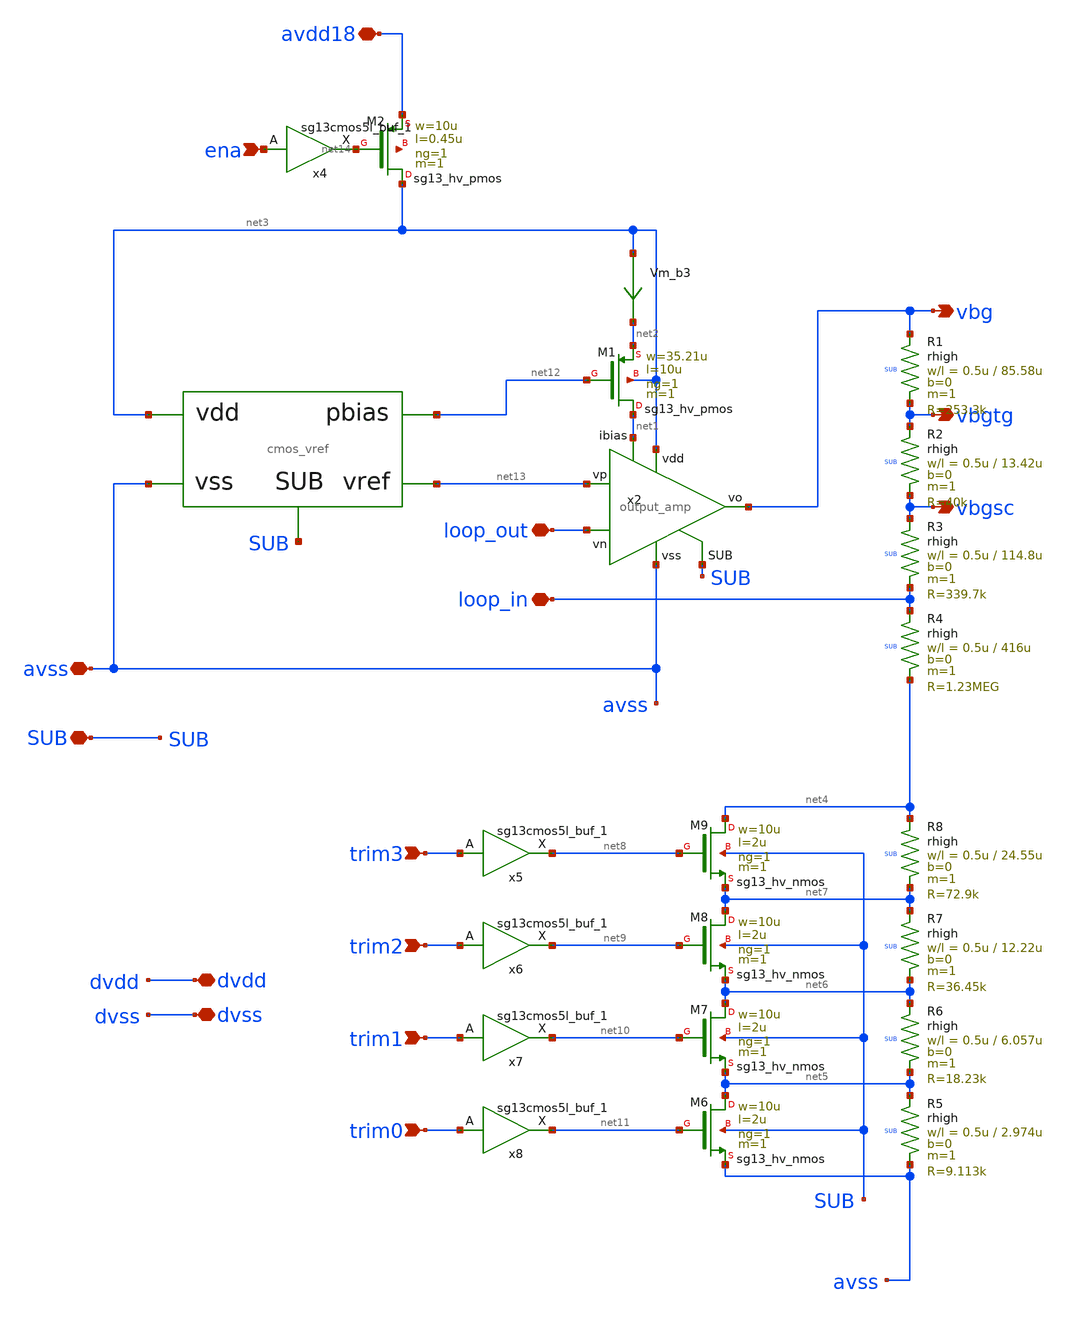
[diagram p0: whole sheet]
** sch_path: release/xschem/sch/top.sch
**.subckt top vbg avss SUB loop_in loop_out dvdd dvss vbgsc vbgtg trim3 trim2 trim1 trim0 avdd18 ena
*.opin vbg
*.iopin avss
*.iopin SUB
*.iopin loop_in
*.iopin loop_out
*.iopin dvdd
*.iopin dvss
*.opin vbgsc
*.opin vbgtg
*.ipin trim3
*.ipin trim2
*.ipin trim1
*.ipin trim0
*.iopin avdd18
*.ipin ena
x2 net3 vbg net13 loop_out net1 avss SUB output_amp
Vm_b3 net3 net2 0
.save i(vm_b3)
XM1 net1 net12 net2 net3 sg13_hv_pmos w=35.21u l=10u ng=1 m=1 mm_ok=1
x5 net8 trim3 dvdd dvss sg13cmos5l_buf_1
x6 net9 trim2 dvdd dvss sg13cmos5l_buf_1
x7 net10 trim1 dvdd dvss sg13cmos5l_buf_1
x8 net11 trim0 dvdd dvss sg13cmos5l_buf_1
XR1 vbg vbgtg SUB rhigh w=0.5u l=85.58u m=1 b=0 mm_ok=1
XR2 vbgtg vbgsc SUB rhigh w=0.5u l=13.42u m=1 b=0 mm_ok=1
XR3 vbgsc loop_in SUB rhigh w=0.5u l=114.8u m=1 b=0 mm_ok=1
XR4 loop_in net4 SUB rhigh w=0.5u l=416u m=1 b=0 mm_ok=1
XM6 net5 net11 avss SUB sg13_hv_nmos w=10u l=2u ng=1 m=1 mm_ok=1
XM7 net6 net10 net5 SUB sg13_hv_nmos w=10u l=2u ng=1 m=1 mm_ok=1
XM8 net7 net9 net6 SUB sg13_hv_nmos w=10u l=2u ng=1 m=1 mm_ok=1
XM9 net4 net8 net7 SUB sg13_hv_nmos w=10u l=2u ng=1 m=1 mm_ok=1
XR5 net5 avss SUB rhigh w=0.5u l=2.974u m=1 b=0 mm_ok=1
XR6 net6 net5 SUB rhigh w=0.5u l=6.057u m=1 b=0 mm_ok=1
XR7 net7 net6 SUB rhigh w=0.5u l=12.22u m=1 b=0 mm_ok=1
XR8 net4 net7 SUB rhigh w=0.5u l=24.55u m=1 b=0 mm_ok=1
X1 net13 net3 avss net12 SUB cmos_vref
x4 net14 ena dvdd dvss sg13cmos5l_buf_1
XM2 net3 net14 avdd18 net15 sg13_hv_pmos w=10u l=0.45u ng=1 m=1 mm_ok=1
**.ends
.end
